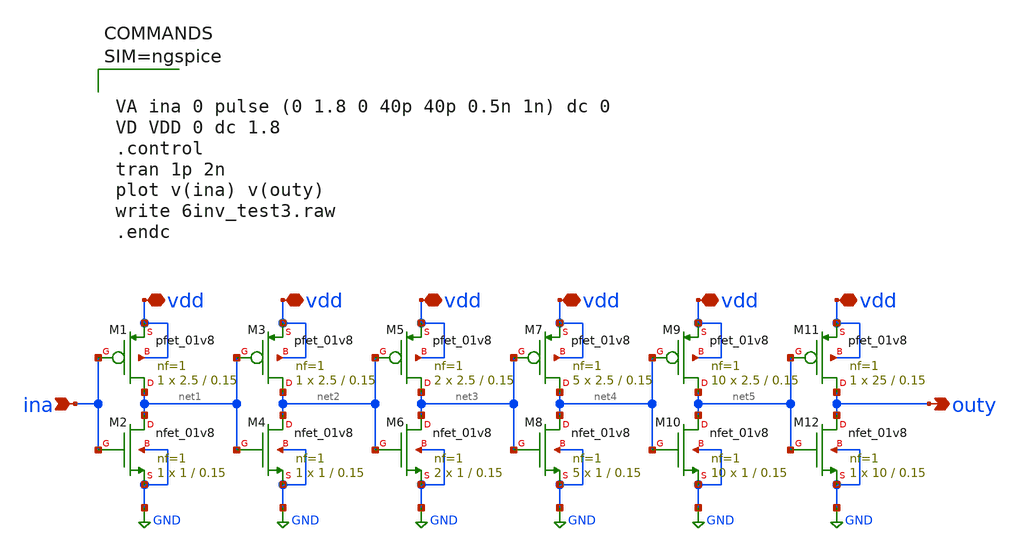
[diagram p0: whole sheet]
** sch_path: 6inv_test.sch
**.subckt 6inv_test vdd ina vdd vdd vdd vdd vdd outy
*.iopin vdd
*.ipin ina
*.iopin vdd
*.iopin vdd
*.iopin vdd
*.iopin vdd
*.iopin vdd
*.opin outy
XM1 net1 ina vdd vdd sky130_fd_pr__pfet_01v8 L=0.15 W=2.5 nf=1 ad='int((nf+1)/2) * W/nf * 0.29' as='int((nf+2)/2) * W/nf * 0.29'
+ pd='2*int((nf+1)/2) * (W/nf + 0.29)' ps='2*int((nf+2)/2) * (W/nf + 0.29)' nrd='0.29 / W' nrs='0.29 / W'
+ sa=0 sb=0 sd=0 mult=1 m=1
XM2 net1 ina GND GND sky130_fd_pr__nfet_01v8 L=0.15 W=1 nf=1 ad='int((nf+1)/2) * W/nf * 0.29' as='int((nf+2)/2) * W/nf * 0.29'
+ pd='2*int((nf+1)/2) * (W/nf + 0.29)' ps='2*int((nf+2)/2) * (W/nf + 0.29)' nrd='0.29 / W' nrs='0.29 / W'
+ sa=0 sb=0 sd=0 mult=1 m=1
XM4 net2 net1 GND GND sky130_fd_pr__nfet_01v8 L=0.15 W=1 nf=1 ad='int((nf+1)/2) * W/nf * 0.29' as='int((nf+2)/2) * W/nf * 0.29'
+ pd='2*int((nf+1)/2) * (W/nf + 0.29)' ps='2*int((nf+2)/2) * (W/nf + 0.29)' nrd='0.29 / W' nrs='0.29 / W'
+ sa=0 sb=0 sd=0 mult=1 m=1
XM6 net3 net2 GND GND sky130_fd_pr__nfet_01v8 L=0.15 W=1 nf=1 ad='int((nf+1)/2) * W/nf * 0.29' as='int((nf+2)/2) * W/nf * 0.29'
+ pd='2*int((nf+1)/2) * (W/nf + 0.29)' ps='2*int((nf+2)/2) * (W/nf + 0.29)' nrd='0.29 / W' nrs='0.29 / W'
+ sa=0 sb=0 sd=0 mult=2 m=2
XM8 net4 net3 GND GND sky130_fd_pr__nfet_01v8 L=0.15 W=1 nf=1 ad='int((nf+1)/2) * W/nf * 0.29' as='int((nf+2)/2) * W/nf * 0.29'
+ pd='2*int((nf+1)/2) * (W/nf + 0.29)' ps='2*int((nf+2)/2) * (W/nf + 0.29)' nrd='0.29 / W' nrs='0.29 / W'
+ sa=0 sb=0 sd=0 mult=5 m=5
XM10 net5 net4 GND GND sky130_fd_pr__nfet_01v8 L=0.15 W=1 nf=1 ad='int((nf+1)/2) * W/nf * 0.29' as='int((nf+2)/2) * W/nf * 0.29'
+ pd='2*int((nf+1)/2) * (W/nf + 0.29)' ps='2*int((nf+2)/2) * (W/nf + 0.29)' nrd='0.29 / W' nrs='0.29 / W'
+ sa=0 sb=0 sd=0 mult=10 m=10
XM12 outy net5 GND GND sky130_fd_pr__nfet_01v8 L=0.15 W=10 nf=1 ad='int((nf+1)/2) * W/nf * 0.29' as='int((nf+2)/2) * W/nf * 0.29'
+ pd='2*int((nf+1)/2) * (W/nf + 0.29)' ps='2*int((nf+2)/2) * (W/nf + 0.29)' nrd='0.29 / W' nrs='0.29 / W'
+ sa=0 sb=0 sd=0 mult=1 m=1
XM3 net2 net1 vdd vdd sky130_fd_pr__pfet_01v8 L=0.15 W=2.5 nf=1 ad='int((nf+1)/2) * W/nf * 0.29' as='int((nf+2)/2) * W/nf * 0.29'
+ pd='2*int((nf+1)/2) * (W/nf + 0.29)' ps='2*int((nf+2)/2) * (W/nf + 0.29)' nrd='0.29 / W' nrs='0.29 / W'
+ sa=0 sb=0 sd=0 mult=1 m=1
XM5 net3 net2 vdd vdd sky130_fd_pr__pfet_01v8 L=0.15 W=2.5 nf=1 ad='int((nf+1)/2) * W/nf * 0.29' as='int((nf+2)/2) * W/nf * 0.29'
+ pd='2*int((nf+1)/2) * (W/nf + 0.29)' ps='2*int((nf+2)/2) * (W/nf + 0.29)' nrd='0.29 / W' nrs='0.29 / W'
+ sa=0 sb=0 sd=0 mult=2 m=2
XM7 net4 net3 vdd vdd sky130_fd_pr__pfet_01v8 L=0.15 W=2.5 nf=1 ad='int((nf+1)/2) * W/nf * 0.29' as='int((nf+2)/2) * W/nf * 0.29'
+ pd='2*int((nf+1)/2) * (W/nf + 0.29)' ps='2*int((nf+2)/2) * (W/nf + 0.29)' nrd='0.29 / W' nrs='0.29 / W'
+ sa=0 sb=0 sd=0 mult=5 m=5
XM9 net5 net4 vdd vdd sky130_fd_pr__pfet_01v8 L=0.15 W=2.5 nf=1 ad='int((nf+1)/2) * W/nf * 0.29' as='int((nf+2)/2) * W/nf * 0.29'
+ pd='2*int((nf+1)/2) * (W/nf + 0.29)' ps='2*int((nf+2)/2) * (W/nf + 0.29)' nrd='0.29 / W' nrs='0.29 / W'
+ sa=0 sb=0 sd=0 mult=10 m=10
XM11 outy net5 vdd vdd sky130_fd_pr__pfet_01v8 L=0.15 W=25 nf=1 ad='int((nf+1)/2) * W/nf * 0.29' as='int((nf+2)/2) * W/nf * 0.29'
+ pd='2*int((nf+1)/2) * (W/nf + 0.29)' ps='2*int((nf+2)/2) * (W/nf + 0.29)' nrd='0.29 / W' nrs='0.29 / W'
+ sa=0 sb=0 sd=0 mult=1 m=1
**** begin user architecture code



VA ina 0 pulse (0 1.8 0 40p 40p 0.5n 1n) dc 0
VD VDD 0 dc 1.8
.control
tran 1p 2n
plot v(ina) v(outy)
write 6inv_test3.raw
.endc




** opencircuitdesign pdks install
.lib $::SKYWATER_MODELS/sky130.lib.spice ss


**** end user architecture code
**.ends
.GLOBAL GND
.end
